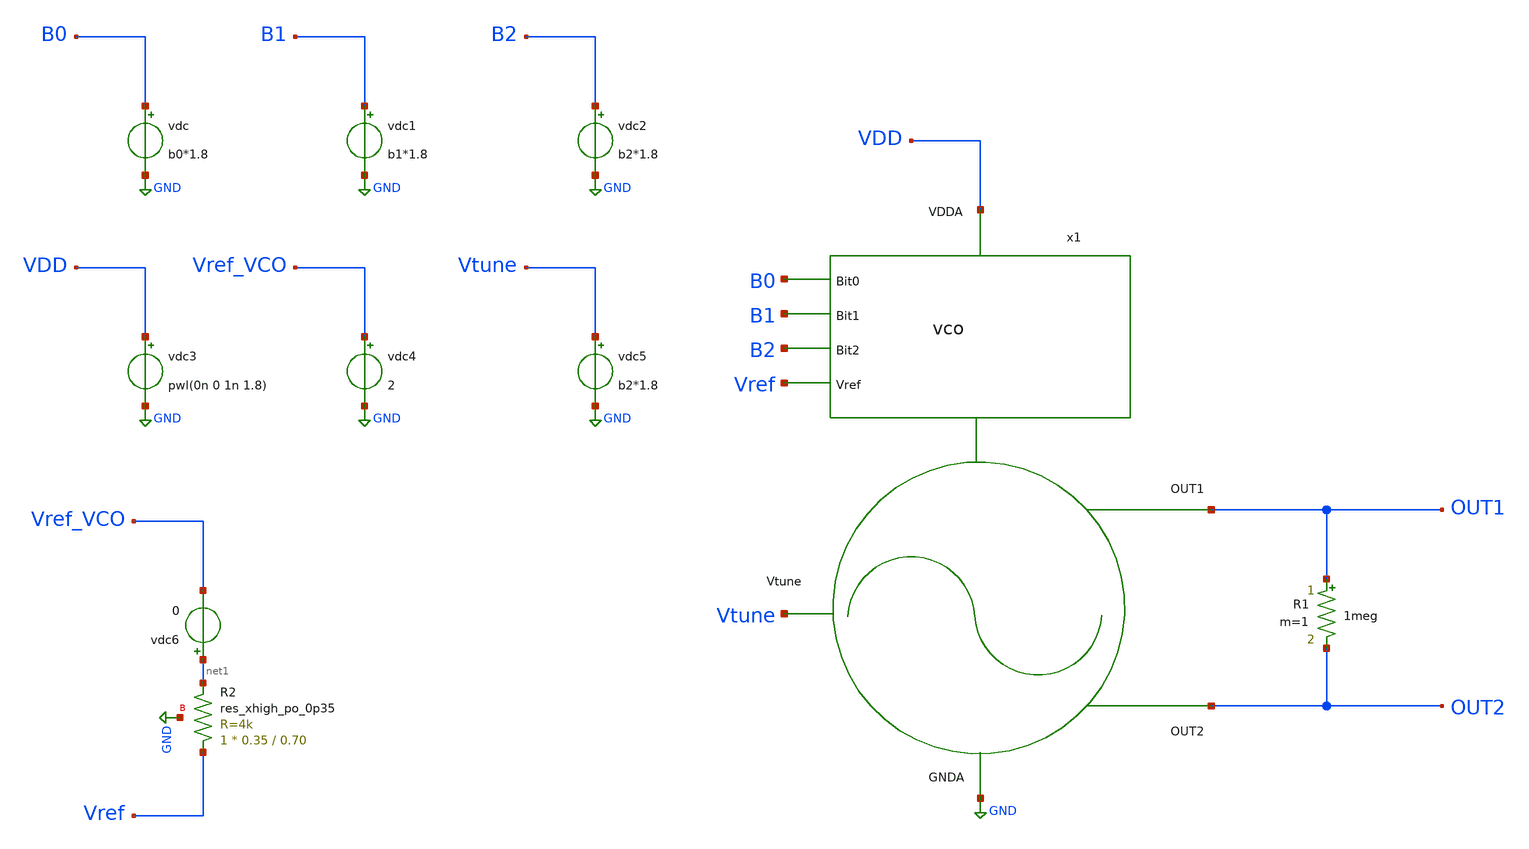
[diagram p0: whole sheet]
** sch_path: projects/pll/vco/xschem_ngspice/tb_vco.sch
**.subckt tb_vco
vdc B0 GND b0*1.8
vdc1 B1 GND b1*1.8
vdc2 B2 GND b2*1.8
vdc3 VDD GND pwl(0n 0 1n 1.8)
vdc4 Vref_VCO GND 2
vdc5 Vtune GND b2*1.8
vdc6 net1 Vref_VCO 0
R1 OUT1 OUT2 1meg m=1
x1 VDD Vtune B0 Vref B1 B2 GND OUT1 OUT2 vco
XR2 Vref net1 GND sky130_fd_pr__res_xhigh_po_0p35 L=0.70 mult=1 m=1
**.ends

* expanding   symbol:  /foss/designs/my_design/projects/pll/vco/xschem_ngspice/vco.sym # of pins=9
** sym_path: projects/pll/vco/xschem_ngspice/vco.sym
** sch_path: projects/pll/vco/xschem_ngspice/vco.sch
.subckt vco VDDA Vtune Bit0 Vref Bit1 Bit2 GNDA OUT1 OUT2
*.ipin GNDA
*.ipin Bit2
*.ipin Bit1
*.ipin Bit0
*.ipin Vtune
*.ipin VDDA
*.ipin Vref
*.opin OUT1
*.opin OUT2
XM9 OUT2 OUT1 GNDA GNDA sky130_fd_pr__nfet_01v8 L=0.18 W=2.5 nf=1 ad='int((nf+1)/2) * W/nf * 0.29' as='int((nf+2)/2) * W/nf * 0.29'
+ pd='2*int((nf+1)/2) * (W/nf + 0.29)' ps='2*int((nf+2)/2) * (W/nf + 0.29)' nrd='0.29 / W' nrs='0.29 / W'
+ sa=0 sb=0 sd=0 mult=5 m=5
XM1 OUT1 OUT2 GNDA GNDA sky130_fd_pr__nfet_01v8 L=0.18 W=2.5 nf=1 ad='int((nf+1)/2) * W/nf * 0.29' as='int((nf+2)/2) * W/nf * 0.29'
+ pd='2*int((nf+1)/2) * (W/nf + 0.29)' ps='2*int((nf+2)/2) * (W/nf + 0.29)' nrd='0.29 / W' nrs='0.29 / W'
+ sa=0 sb=0 sd=0 mult=5 m=5
XM2 OUT2 OUT1 net3 VDDA sky130_fd_pr__pfet_01v8 L=0.18 W=5 nf=1 ad='int((nf+1)/2) * W/nf * 0.29' as='int((nf+2)/2) * W/nf * 0.29'
+ pd='2*int((nf+1)/2) * (W/nf + 0.29)' ps='2*int((nf+2)/2) * (W/nf + 0.29)' nrd='0.29 / W' nrs='0.29 / W'
+ sa=0 sb=0 sd=0 mult=15 m=15
XM3 OUT1 OUT2 net3 VDDA sky130_fd_pr__pfet_01v8 L=0.18 W=5 nf=1 ad='int((nf+1)/2) * W/nf * 0.29' as='int((nf+2)/2) * W/nf * 0.29'
+ pd='2*int((nf+1)/2) * (W/nf + 0.29)' ps='2*int((nf+2)/2) * (W/nf + 0.29)' nrd='0.29 / W' nrs='0.29 / W'
+ sa=0 sb=0 sd=0 mult=15 m=15
XM4 net3 net1 VDDA VDDA sky130_fd_pr__pfet_01v8 L=1.5 W=10 nf=1 ad='int((nf+1)/2) * W/nf * 0.29' as='int((nf+2)/2) * W/nf * 0.29'
+ pd='2*int((nf+1)/2) * (W/nf + 0.29)' ps='2*int((nf+2)/2) * (W/nf + 0.29)' nrd='0.29 / W' nrs='0.29 / W'
+ sa=0 sb=0 sd=0 mult=150 m=150
XM5 net1 net1 VDDA VDDA sky130_fd_pr__pfet_01v8 L=1.5 W=10 nf=1 ad='int((nf+1)/2) * W/nf * 0.29' as='int((nf+2)/2) * W/nf * 0.29'
+ pd='2*int((nf+1)/2) * (W/nf + 0.29)' ps='2*int((nf+2)/2) * (W/nf + 0.29)' nrd='0.29 / W' nrs='0.29 / W'
+ sa=0 sb=0 sd=0 mult=10 m=10
XM6 net1 net2 GNDA GNDA sky130_fd_pr__nfet_01v8 L=0.18 W=15 nf=1 ad='int((nf+1)/2) * W/nf * 0.29' as='int((nf+2)/2) * W/nf * 0.29'
+ pd='2*int((nf+1)/2) * (W/nf + 0.29)' ps='2*int((nf+2)/2) * (W/nf + 0.29)' nrd='0.29 / W' nrs='0.29 / W'
+ sa=0 sb=0 sd=0 mult=10 m=10
XM7 net2 net2 GNDA GNDA sky130_fd_pr__nfet_01v8 L=0.18 W=15 nf=1 ad='int((nf+1)/2) * W/nf * 0.29' as='int((nf+2)/2) * W/nf * 0.29'
+ pd='2*int((nf+1)/2) * (W/nf + 0.29)' ps='2*int((nf+2)/2) * (W/nf + 0.29)' nrd='0.29 / W' nrs='0.29 / W'
+ sa=0 sb=0 sd=0 mult=10 m=10
XR3 net2 Vref GNDA sky130_fd_pr__res_xhigh_po_0p35 L=0.70 mult=1 m=1
XC8 OUT1 Bit2 GNDA sky130_fd_pr__cap_var_lvt W=9.6 L=5.3 VM=1 m=1
XC1 OUT2 Bit2 GNDA sky130_fd_pr__cap_var_lvt W=9.6 L=5.3 VM=1 m=1
XC2 OUT1 Bit1 GNDA sky130_fd_pr__cap_var_lvt W=5.4 L=4.5 VM=1 m=1
XC3 OUT2 Bit1 GNDA sky130_fd_pr__cap_var_lvt W=5.4 L=4.5 VM=1 m=1
XC4 OUT1 Bit0 GNDA sky130_fd_pr__cap_var_lvt W=3.6 L=3.4 VM=1 m=1
XC5 OUT2 Bit0 GNDA sky130_fd_pr__cap_var_lvt W=3.6 L=3.4 VM=1 m=1
XC6 OUT1 Vtune GNDA sky130_fd_pr__cap_var_lvt W=6.5 L=5.6 VM=1 m=1
XC7 OUT2 Vtune GNDA sky130_fd_pr__cap_var_lvt W=6.5 L=5.6 VM=1 m=1
XC11 OUT1 net4 sky130_fd_pr__cap_mim_m3_1 W=22 L=16 MF=1 m=1
XC9 OUT2 net4 sky130_fd_pr__cap_mim_m3_1 W=22 L=16 MF=1 m=1
L2 OUT2 OUT1 996.029p m=1
.ends

.GLOBAL GND
.end
